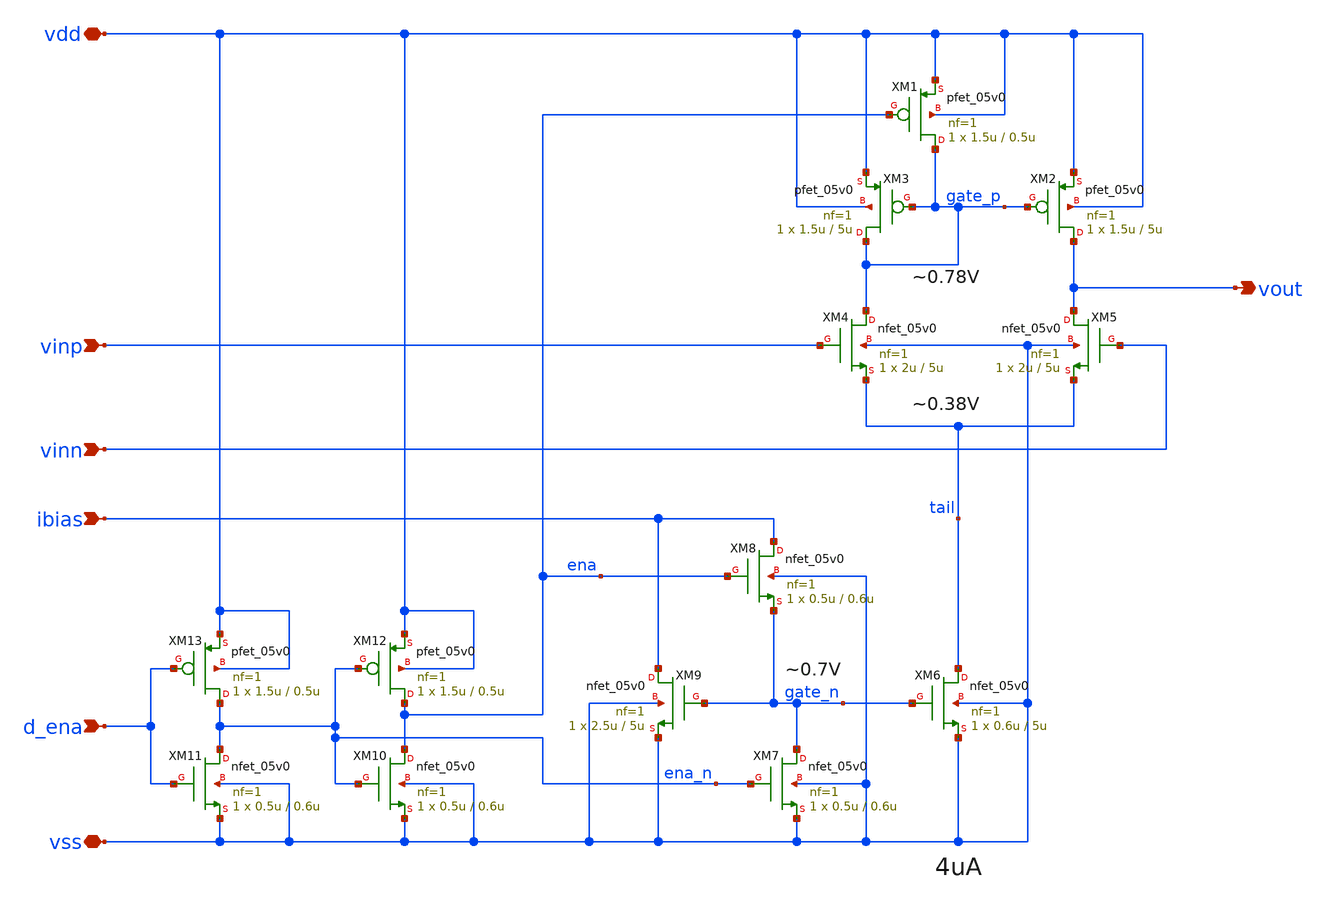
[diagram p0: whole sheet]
** sch_path: xschem_dev_ghaith/ota-5t.sch
**.subckt ota-5t ibias vdd vss vinp vinn vout d_ena
*.ipin ibias
*.iopin vdd
*.iopin vss
*.ipin vinp
*.ipin vinn
*.opin vout
*.ipin d_ena
XM1 gate_p ena vdd vdd pfet_05v0 L=0.5u W=1.5u nf=1 ad='int((nf+1)/2) * W/nf * 0.18u' as='int((nf+2)/2) * W/nf * 0.18u'
+ pd='2*int((nf+1)/2) * (W/nf + 0.18u)' ps='2*int((nf+2)/2) * (W/nf + 0.18u)' nrd='0.18u / W' nrs='0.18u / W'
+ sa=0 sb=0 sd=0 m=1
XM2 vout gate_p vdd vdd pfet_05v0 L=5u W=1.5u nf=1 ad='int((nf+1)/2) * W/nf * 0.18u' as='int((nf+2)/2) * W/nf * 0.18u'
+ pd='2*int((nf+1)/2) * (W/nf + 0.18u)' ps='2*int((nf+2)/2) * (W/nf + 0.18u)' nrd='0.18u / W' nrs='0.18u / W'
+ sa=0 sb=0 sd=0 m=1
XM3 gate_p gate_p vdd vdd pfet_05v0 L=5u W=1.5u nf=1 ad='int((nf+1)/2) * W/nf * 0.18u' as='int((nf+2)/2) * W/nf * 0.18u'
+ pd='2*int((nf+1)/2) * (W/nf + 0.18u)' ps='2*int((nf+2)/2) * (W/nf + 0.18u)' nrd='0.18u / W' nrs='0.18u / W'
+ sa=0 sb=0 sd=0 m=1
XM4 gate_p vinp tail vss nfet_05v0 L=5u W=2u nf=1 ad='int((nf+1)/2) * W/nf * 0.18u' as='int((nf+2)/2) * W/nf * 0.18u'
+ pd='2*int((nf+1)/2) * (W/nf + 0.18u)' ps='2*int((nf+2)/2) * (W/nf + 0.18u)' nrd='0.18u / W' nrs='0.18u / W'
+ sa=0 sb=0 sd=0 m=1
XM5 vout vinn tail vss nfet_05v0 L=5u W=2u nf=1 ad='int((nf+1)/2) * W/nf * 0.18u' as='int((nf+2)/2) * W/nf * 0.18u'
+ pd='2*int((nf+1)/2) * (W/nf + 0.18u)' ps='2*int((nf+2)/2) * (W/nf + 0.18u)' nrd='0.18u / W' nrs='0.18u / W'
+ sa=0 sb=0 sd=0 m=1
XM6 tail gate_n vss vss nfet_05v0 L=5u W=0.6u nf=1 ad='int((nf+1)/2) * W/nf * 0.18u' as='int((nf+2)/2) * W/nf * 0.18u'
+ pd='2*int((nf+1)/2) * (W/nf + 0.18u)' ps='2*int((nf+2)/2) * (W/nf + 0.18u)' nrd='0.18u / W' nrs='0.18u / W'
+ sa=0 sb=0 sd=0 m=1
XM7 gate_n ena_n vss vss nfet_05v0 L=0.6u W=0.5u nf=1 ad='int((nf+1)/2) * W/nf * 0.18u' as='int((nf+2)/2) * W/nf * 0.18u'
+ pd='2*int((nf+1)/2) * (W/nf + 0.18u)' ps='2*int((nf+2)/2) * (W/nf + 0.18u)' nrd='0.18u / W' nrs='0.18u / W'
+ sa=0 sb=0 sd=0 m=1
XM8 ibias ena gate_n vss nfet_05v0 L=0.6u W=0.5u nf=1 ad='int((nf+1)/2) * W/nf * 0.18u' as='int((nf+2)/2) * W/nf * 0.18u'
+ pd='2*int((nf+1)/2) * (W/nf + 0.18u)' ps='2*int((nf+2)/2) * (W/nf + 0.18u)' nrd='0.18u / W' nrs='0.18u / W'
+ sa=0 sb=0 sd=0 m=1
XM9 ibias gate_n vss vss nfet_05v0 L=5u W=2.5u nf=1 ad='int((nf+1)/2) * W/nf * 0.18u' as='int((nf+2)/2) * W/nf * 0.18u'
+ pd='2*int((nf+1)/2) * (W/nf + 0.18u)' ps='2*int((nf+2)/2) * (W/nf + 0.18u)' nrd='0.18u / W' nrs='0.18u / W'
+ sa=0 sb=0 sd=0 m=1
XM10 ena ena_n vss vss nfet_05v0 L=0.6u W=0.5u nf=1 ad='int((nf+1)/2) * W/nf * 0.18u' as='int((nf+2)/2) * W/nf * 0.18u'
+ pd='2*int((nf+1)/2) * (W/nf + 0.18u)' ps='2*int((nf+2)/2) * (W/nf + 0.18u)' nrd='0.18u / W' nrs='0.18u / W'
+ sa=0 sb=0 sd=0 m=1
XM11 ena_n d_ena vss vss nfet_05v0 L=0.6u W=0.5u nf=1 ad='int((nf+1)/2) * W/nf * 0.18u' as='int((nf+2)/2) * W/nf * 0.18u'
+ pd='2*int((nf+1)/2) * (W/nf + 0.18u)' ps='2*int((nf+2)/2) * (W/nf + 0.18u)' nrd='0.18u / W' nrs='0.18u / W'
+ sa=0 sb=0 sd=0 m=1
XM12 ena ena_n vdd vdd pfet_05v0 L=0.5u W=1.5u nf=1 ad='int((nf+1)/2) * W/nf * 0.18u' as='int((nf+2)/2) * W/nf * 0.18u'
+ pd='2*int((nf+1)/2) * (W/nf + 0.18u)' ps='2*int((nf+2)/2) * (W/nf + 0.18u)' nrd='0.18u / W' nrs='0.18u / W'
+ sa=0 sb=0 sd=0 m=1
XM13 ena_n d_ena vdd vdd pfet_05v0 L=0.5u W=1.5u nf=1 ad='int((nf+1)/2) * W/nf * 0.18u' as='int((nf+2)/2) * W/nf * 0.18u'
+ pd='2*int((nf+1)/2) * (W/nf + 0.18u)' ps='2*int((nf+2)/2) * (W/nf + 0.18u)' nrd='0.18u / W' nrs='0.18u / W'
+ sa=0 sb=0 sd=0 m=1
**.ends
.end
